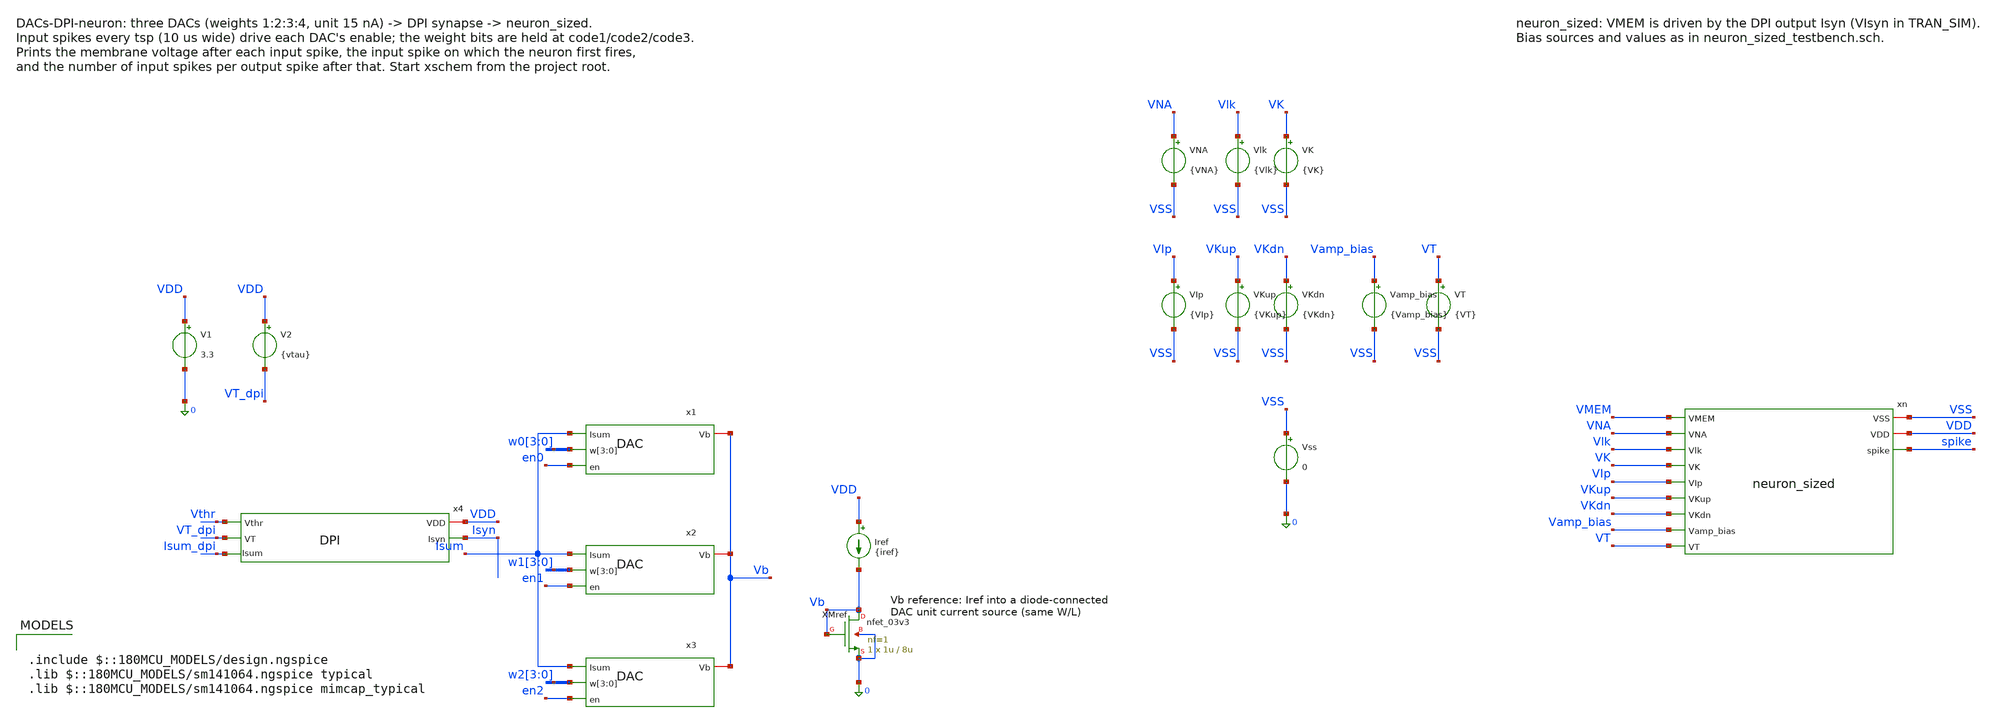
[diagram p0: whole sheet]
** sch_path: analog/neuron/DACs-DPI-neuron.sch
**.subckt DACs-DPI-neuron
x1 Isum Vb w0[3] w0[2] w0[1] w0[0] en0 DAC
x2 Isum Vb w1[3] w1[2] w1[1] w1[0] en1 DAC
x3 Isum Vb w2[3] w2[2] w2[1] w2[0] en2 DAC
x4 VDD Vthr Isyn Isum_dpi VT_dpi DPI
Iref VDD Vb {iref}
XMref Vb Vb 0 0 nfet_03v3 L=8u W=1u nf=1 ad='int((nf+1)/2) * W/nf * 0.18u' as='int((nf+2)/2) * W/nf * 0.18u'
+ pd='2*int((nf+1)/2) * (W/nf + 0.18u)' ps='2*int((nf+2)/2) * (W/nf + 0.18u)' nrd='0.18u / W' nrs='0.18u / W'
+ sa=0 sb=0 sd=0 m=1
V1 VDD 0 3.3
V2 VDD VT_dpi {vtau}
Vss VSS 0 0
xn VSS VDD VMEM VNA Vlk VK VIp VKup VKdn Vamp_bias VT spike neuron_sized
Vlk Vlk VSS {Vlk}
VK VK VSS {VK}
VNA VNA VSS {VNA}
VKup VKup VSS {VKup}
VKdn VKdn VSS {VKdn}
VIp VIp VSS {VIp}
VT VT VSS {VT}
Vamp_bias Vamp_bias VSS {Vamp_bias}
**** begin user architecture code

.include $::180MCU_MODELS/design.ngspice
.lib $::180MCU_MODELS/sm141064.ngspice typical
.lib $::180MCU_MODELS/sm141064.ngspice mimcap_typical



* How many input spikes of a given weight fire neuron_sized.
* One input spike of width tpw every tsp, from t0, on the enable (en) of each DAC.
* The weight bits of DACs x1 / x2 / x3 are held at code1 / code2 / code3 (0..15). DAC branch weights
*+ w[0]..w[3] = 1:2:3:4 with a 15 nA unit,
* so code 2 = weight 2 = 30 nA while the spike is high.
* vthr is tuned so that code 2 at 5 kHz (tsp = 200 us) first fires the neuron on input
* spike 10 (tt, 27 C). The count is steep in vthr: about one input spike per 1-2 mV.
.param vdd=3.3 vthr=2.909 vtau=0.40 iref=14.42n tpw=10u tsp=200u t0=100u
.param code1=2 code2=0 code3=0
* neuron_sized biases, as in neuron_sized_testbench.sch
.param Vlk=0.425 Vamp_bias=0.535 VIp=0.573 VNA=1.93 VKup=2.35 VK=1.22 VKdn=0.588 VT=1.66
* Bit b of each code
.param x1b0={code1-2*floor(code1/2)} x1b1={floor(code1/2)-2*floor(code1/4)}
.param x1b2={floor(code1/4)-2*floor(code1/8)} x1b3={floor(code1/8)-2*floor(code1/16)}
.param x2b0={code2-2*floor(code2/2)} x2b1={floor(code2/2)-2*floor(code2/4)}
.param x2b2={floor(code2/4)-2*floor(code2/8)} x2b3={floor(code2/8)-2*floor(code2/16)}
.param x3b0={code3-2*floor(code3/2)} x3b1={floor(code3/2)-2*floor(code3/4)}
.param x3b2={floor(code3/4)-2*floor(code3/8)} x3b3={floor(code3/8)-2*floor(code3/16)}
.csparam tsp_c={tsp}
.csparam t0_c={t0}
.csparam wsum_c={x1b0+2*x1b1+3*x1b2+4*x1b3 + x2b0+2*x2b1+3*x2b2+4*x2b3 + x3b0+2*x3b1+3*x3b2+4*x3b3}
.ic v(VMEM)=0 v(spike)=0
* Gear integration: the default (trap) makes i(VIsyn) ring step to step after each reset
.options method=gear

Vthr  Vthr 0 {vthr}
VIdac Isum_dpi Isum 0
* DPI output into the neuron membrane
VIsyn Isyn VMEM 0

* Weights are static levels, as from the weight register file: Vw<b><d> holds
* bit <b> of code<d+1> on DAC x<d+1> (net w<d>[<b>])
Vw00 w0[0] 0 {vdd*x1b0}
Vw10 w0[1] 0 {vdd*x1b1}
Vw20 w0[2] 0 {vdd*x1b2}
Vw30 w0[3] 0 {vdd*x1b3}
Vw01 w1[0] 0 {vdd*x2b0}
Vw11 w1[1] 0 {vdd*x2b1}
Vw21 w1[2] 0 {vdd*x2b2}
Vw31 w1[3] 0 {vdd*x2b3}
Vw02 w2[0] 0 {vdd*x3b0}
Vw12 w2[1] 0 {vdd*x3b1}
Vw22 w2[2] 0 {vdd*x3b2}
Vw32 w2[3] 0 {vdd*x3b3}

* Input spike train on each DAC's enable (the previous section's output)
Ven0 en0 0 pulse(0 {vdd} {t0} 10n 10n {tpw} {tsp})
Ven1 en1 0 pulse(0 {vdd} {t0} 10n 10n {tpw} {tsp})
Ven2 en2 0 pulse(0 {vdd} {t0} 10n 10n {tpw} {tsp})

.control
  save all
  set wr_singlescale
  set wr_vecnames
  tran 0.1u 6.1m 0 0.5u
  let isyn = i(VIsyn)
  let nin = floor((6.1m - t0_c)/tsp_c)
  let rate_khz = 1e-3/tsp_c
  echo
  echo Total weight per input spike: $&wsum_c, input rate $&rate_khz kHz, $&nin input spikes

  meas tran vsp max v(spike)
  let n_first = 0
  if vsp < 1.65
    echo The neuron did not fire.
    let nshow = nin
  else
    meas tran t1 when v(spike)=1.65 rise=1
    let n_first = floor((t1 - t0_c)/tsp_c) + 1
    let lat_us = (t1 - t0_c - (n_first - 1)*tsp_c)*1e6
    let nshow = n_first
    echo First output spike after input spike $&n_first ($&lat_us us after it).
  end

  * Membrane just before each next input spike, and the DPI peak in each interval
  echo
  echo input  VMEM_before_next(V)  Isyn_peak(nA)
  let k = 1
  while k <= nshow
    let ta = t0_c + (k - 1)*tsp_c
    let tb = t0_c + k*tsp_c - 1u
    meas tran m_v find v(VMEM) at=$&tb
    let tc = ta + 0.5*tsp_c
    meas tran m_i max isyn from=$&ta to=$&tc
    let i_na = m_i*1e9
    if k = n_first
      echo $&k  fired  $&i_na
    else
      echo $&k  $&m_v  $&i_na
    end
    let k = k + 1
  end

  * Input spikes per output spike once firing has started
  let t3 = 0
  if n_first > 0
    meas tran t3 when v(spike)=1.65 rise=3
  end
  let n_per = 0
  if t3 > 0
    let n_per = (t3 - t1)/(2*tsp_c)
    echo
    echo After the first output: one output spike every $&n_per input spikes.
  end

  * DAC charge per input spike (spike 2), with the DAC leakage between spikes removed
  let ta = t0_c + tsp_c
  let tm = ta + 0.5*tsp_c
  let te = ta + tsp_c - 1u
  meas tran m_q integ i(VIdac) from=$&ta to=$&tm
  meas tran m_lk avg i(VIdac) from=$&tm to=$&te
  let q_spike = m_q - m_lk*(tm - ta)
  let q_fc = q_spike*1e15
  let lk_pa = m_lk*1e12
  echo DAC charge per input spike: $&q_fc fC (DAC leakage between spikes $&lk_pa pA)
  echo RES q_spike=$&q_spike
  echo RES i_leak=$&m_lk

  echo RES n_first=$&n_first
  echo RES n_per=$&n_per

  wrdata dacs_dpi_neuron.txt v(VMEM) v(spike) isyn v(en0)
  if $?batchmode = 0
    plot v(VMEM) v(spike) v(en0)*0.15 title 'Membrane, output spike, input spikes on en0 (x0.15)' ylabel
+ 'V'
    plot isyn title 'DPI output current into the membrane' ylabel 'A'
  end
.endc


**** end user architecture code
**.ends

* expanding   symbol:  DAC.sym # of pins=4
** sym_path: analog/neuron/DAC.sym
** sch_path: analog/neuron/DAC.sch
.subckt DAC Isum Vb w[3] w[2] w[1] w[0] en
*.iopin Vb
*.ipin w[3],w[2],w[1],w[0]
*.ipin Isum
*.ipin en
XM1 X w[0] net4 net4 nfet_03v3 L=0.28u W=0.22u nf=1 ad='int((nf+1)/2) * W/nf * 0.18u' as='int((nf+2)/2) * W/nf * 0.18u'
+ pd='2*int((nf+1)/2) * (W/nf + 0.18u)' ps='2*int((nf+2)/2) * (W/nf + 0.18u)' nrd='0.18u / W' nrs='0.18u / W'
+ sa=0 sb=0 sd=0 m=1
XM2 net4 Vb GND GND nfet_03v3 L=8u W=1u nf=1 ad='int((nf+1)/2) * W/nf * 0.18u' as='int((nf+2)/2) * W/nf * 0.18u'
+ pd='2*int((nf+1)/2) * (W/nf + 0.18u)' ps='2*int((nf+2)/2) * (W/nf + 0.18u)' nrd='0.18u / W' nrs='0.18u / W'
+ sa=0 sb=0 sd=0 m=1
XM3 X w[1] net2 net2 nfet_03v3 L=0.28u W=0.22u nf=1 ad='int((nf+1)/2) * W/nf * 0.18u' as='int((nf+2)/2) * W/nf * 0.18u'
+ pd='2*int((nf+1)/2) * (W/nf + 0.18u)' ps='2*int((nf+2)/2) * (W/nf + 0.18u)' nrd='0.18u / W' nrs='0.18u / W'
+ sa=0 sb=0 sd=0 m=2
XM4 net2 Vb GND GND nfet_03v3 L=8u W=1u nf=1 ad='int((nf+1)/2) * W/nf * 0.18u' as='int((nf+2)/2) * W/nf * 0.18u'
+ pd='2*int((nf+1)/2) * (W/nf + 0.18u)' ps='2*int((nf+2)/2) * (W/nf + 0.18u)' nrd='0.18u / W' nrs='0.18u / W'
+ sa=0 sb=0 sd=0 m=2
XM5 X w[2] net3 net3 nfet_03v3 L=0.28u W=0.22u nf=1 ad='int((nf+1)/2) * W/nf * 0.18u' as='int((nf+2)/2) * W/nf * 0.18u'
+ pd='2*int((nf+1)/2) * (W/nf + 0.18u)' ps='2*int((nf+2)/2) * (W/nf + 0.18u)' nrd='0.18u / W' nrs='0.18u / W'
+ sa=0 sb=0 sd=0 m=3
XM6 net3 Vb GND GND nfet_03v3 L=8u W=1u nf=1 ad='int((nf+1)/2) * W/nf * 0.18u' as='int((nf+2)/2) * W/nf * 0.18u'
+ pd='2*int((nf+1)/2) * (W/nf + 0.18u)' ps='2*int((nf+2)/2) * (W/nf + 0.18u)' nrd='0.18u / W' nrs='0.18u / W'
+ sa=0 sb=0 sd=0 m=3
XM7 X w[3] net1 net1 nfet_03v3 L=0.28u W=0.22u nf=1 ad='int((nf+1)/2) * W/nf * 0.18u' as='int((nf+2)/2) * W/nf * 0.18u'
+ pd='2*int((nf+1)/2) * (W/nf + 0.18u)' ps='2*int((nf+2)/2) * (W/nf + 0.18u)' nrd='0.18u / W' nrs='0.18u / W'
+ sa=0 sb=0 sd=0 m=4
XM8 net1 Vb GND GND nfet_03v3 L=8u W=1u nf=1 ad='int((nf+1)/2) * W/nf * 0.18u' as='int((nf+2)/2) * W/nf * 0.18u'
+ pd='2*int((nf+1)/2) * (W/nf + 0.18u)' ps='2*int((nf+2)/2) * (W/nf + 0.18u)' nrd='0.18u / W' nrs='0.18u / W'
+ sa=0 sb=0 sd=0 m=4
XMen Isum en X GND nfet_03v3 L=0.28u W=0.22u nf=1 ad='int((nf+1)/2) * W/nf * 0.18u' as='int((nf+2)/2) * W/nf * 0.18u'
+ pd='2*int((nf+1)/2) * (W/nf + 0.18u)' ps='2*int((nf+2)/2) * (W/nf + 0.18u)' nrd='0.18u / W' nrs='0.18u / W'
+ sa=0 sb=0 sd=0 m=1
.ends


* expanding   symbol:  DPI.sym # of pins=5
** sym_path: analog/neuron/DPI.sym
** sch_path: analog/neuron/DPI.sch
.subckt DPI VDD Vthr Isyn Isum VT
*.ipin Vthr
*.iopin VDD
*.opin Isyn
*.opin Isum
*.ipin VT
XM1 VDD Vthr Isum Isum nfet_03v3 L=0.28u W=0.22u nf=1 ad='int((nf+1)/2) * W/nf * 0.18u' as='int((nf+2)/2) * W/nf * 0.18u'
+ pd='2*int((nf+1)/2) * (W/nf + 0.18u)' ps='2*int((nf+2)/2) * (W/nf + 0.18u)' nrd='0.18u / W' nrs='0.18u / W'
+ sa=0 sb=0 sd=0 m=1
XM2 net1 net1 Isum Isum nfet_03v3 L=0.28u W=0.22u nf=1 ad='int((nf+1)/2) * W/nf * 0.18u' as='int((nf+2)/2) * W/nf * 0.18u'
+ pd='2*int((nf+1)/2) * (W/nf + 0.18u)' ps='2*int((nf+2)/2) * (W/nf + 0.18u)' nrd='0.18u / W' nrs='0.18u / W'
+ sa=0 sb=0 sd=0 m=1
XM3 net1 VT VDD VDD pfet_03v3 L=0.28u W=0.22u nf=1 ad='int((nf+1)/2) * W/nf * 0.18u' as='int((nf+2)/2) * W/nf * 0.18u'
+ pd='2*int((nf+1)/2) * (W/nf + 0.18u)' ps='2*int((nf+2)/2) * (W/nf + 0.18u)' nrd='0.18u / W' nrs='0.18u / W'
+ sa=0 sb=0 sd=0 m=1
XM4 Isyn net1 VDD VDD pfet_03v3 L=0.28u W=0.22u nf=1 ad='int((nf+1)/2) * W/nf * 0.18u' as='int((nf+2)/2) * W/nf * 0.18u'
+ pd='2*int((nf+1)/2) * (W/nf + 0.18u)' ps='2*int((nf+2)/2) * (W/nf + 0.18u)' nrd='0.18u / W' nrs='0.18u / W'
+ sa=0 sb=0 sd=0 m=1
C4 VDD net1 1p m=1
.ends


* expanding   symbol:  neuron_sized.sym # of pins=12
** sym_path: analog/neuron/neuron_sized.sym
** sch_path: analog/neuron/neuron_sized.sch
.subckt neuron_sized VSS VDD VMEM VNA Vlk VK VIp VKup VKdn Vamp_bias VT spike
*.iopin VSS
*.iopin VDD
*.ipin VMEM
*.ipin VNA
*.ipin Vlk
*.ipin VK
*.ipin VIp
*.ipin VKup
*.ipin VKdn
*.opin spike
*.ipin Vamp_bias
*.ipin VT
x1 VDD VSS VMEM VT Vamp_bias net1 spike_amplifier
XM1 net2 net1 net4 VSS nfet_03v3 L=0.28u W=0.22u nf=1 ad='int((nf+1)/2) * W/nf * 0.18u' as='int((nf+2)/2) * W/nf * 0.18u'
+ pd='2*int((nf+1)/2) * (W/nf + 0.18u)' ps='2*int((nf+2)/2) * (W/nf + 0.18u)' nrd='0.18u / W' nrs='0.18u / W'
+ sa=0 sb=0 sd=0 m=1
XM2 spike net2 net5 VSS nfet_03v3 L=0.28u W=0.22u nf=1 ad='int((nf+1)/2) * W/nf * 0.18u' as='int((nf+2)/2) * W/nf * 0.18u'
+ pd='2*int((nf+1)/2) * (W/nf + 0.18u)' ps='2*int((nf+2)/2) * (W/nf + 0.18u)' nrd='0.18u / W' nrs='0.18u / W'
+ sa=0 sb=0 sd=0 m=1
XM3 net2 net1 VDD VDD pfet_03v3 L=0.28u W=0.22u nf=1 ad='int((nf+1)/2) * W/nf * 0.18u' as='int((nf+2)/2) * W/nf * 0.18u'
+ pd='2*int((nf+1)/2) * (W/nf + 0.18u)' ps='2*int((nf+2)/2) * (W/nf + 0.18u)' nrd='0.18u / W' nrs='0.18u / W'
+ sa=0 sb=0 sd=0 m=1
XM4 spike net2 net3 VDD pfet_03v3 L=0.28u W=0.22u nf=1 ad='int((nf+1)/2) * W/nf * 0.18u' as='int((nf+2)/2) * W/nf * 0.18u'
+ pd='2*int((nf+1)/2) * (W/nf + 0.18u)' ps='2*int((nf+2)/2) * (W/nf + 0.18u)' nrd='0.18u / W' nrs='0.18u / W'
+ sa=0 sb=0 sd=0 m=1
XM5 VMEM net2 net7 VDD pfet_03v3 L=0.28u W=0.22u nf=1 ad='int((nf+1)/2) * W/nf * 0.18u' as='int((nf+2)/2) * W/nf * 0.18u'
+ pd='2*int((nf+1)/2) * (W/nf + 0.18u)' ps='2*int((nf+2)/2) * (W/nf + 0.18u)' nrd='0.18u / W' nrs='0.18u / W'
+ sa=0 sb=0 sd=0 m=1
XM6 VMEM spike net6 VSS nfet_03v3 L=5u W=0.22u nf=1 ad='int((nf+1)/2) * W/nf * 0.18u' as='int((nf+2)/2) * W/nf * 0.18u'
+ pd='2*int((nf+1)/2) * (W/nf + 0.18u)' ps='2*int((nf+2)/2) * (W/nf + 0.18u)' nrd='0.18u / W' nrs='0.18u / W'
+ sa=0 sb=0 sd=0 m=1
XC1 spike VSS cap_mim_2f0_m3m4_noshield c_width=10e-6 c_length=10e-6 m=1
XM7 net5 VKdn VSS VSS nfet_03v3 L=1u W=1u nf=1 ad='int((nf+1)/2) * W/nf * 0.18u' as='int((nf+2)/2) * W/nf * 0.18u'
+ pd='2*int((nf+1)/2) * (W/nf + 0.18u)' ps='2*int((nf+2)/2) * (W/nf + 0.18u)' nrd='0.18u / W' nrs='0.18u / W'
+ sa=0 sb=0 sd=0 m=1
XM8 net4 VIp VSS VSS nfet_03v3 L=1u W=1u nf=1 ad='int((nf+1)/2) * W/nf * 0.18u' as='int((nf+2)/2) * W/nf * 0.18u'
+ pd='2*int((nf+1)/2) * (W/nf + 0.18u)' ps='2*int((nf+2)/2) * (W/nf + 0.18u)' nrd='0.18u / W' nrs='0.18u / W'
+ sa=0 sb=0 sd=0 m=1
XM9 net7 VNA VDD VDD pfet_03v3 L=1u W=1u nf=1 ad='int((nf+1)/2) * W/nf * 0.18u' as='int((nf+2)/2) * W/nf * 0.18u'
+ pd='2*int((nf+1)/2) * (W/nf + 0.18u)' ps='2*int((nf+2)/2) * (W/nf + 0.18u)' nrd='0.18u / W' nrs='0.18u / W'
+ sa=0 sb=0 sd=0 m=1
XM10 net6 VK VSS VSS nfet_03v3 L=1u W=1u nf=1 ad='int((nf+1)/2) * W/nf * 0.18u' as='int((nf+2)/2) * W/nf * 0.18u'
+ pd='2*int((nf+1)/2) * (W/nf + 0.18u)' ps='2*int((nf+2)/2) * (W/nf + 0.18u)' nrd='0.18u / W' nrs='0.18u / W'
+ sa=0 sb=0 sd=0 m=1
XC2 VMEM VSS cap_mim_2f0_m3m4_noshield c_width=22.18e-6 c_length=22.18e-6 m=1
XM11 VMEM Vlk VSS VSS nfet_03v3 L=1u W=1u nf=1 ad='int((nf+1)/2) * W/nf * 0.18u' as='int((nf+2)/2) * W/nf * 0.18u'
+ pd='2*int((nf+1)/2) * (W/nf + 0.18u)' ps='2*int((nf+2)/2) * (W/nf + 0.18u)' nrd='0.18u / W' nrs='0.18u / W'
+ sa=0 sb=0 sd=0 m=1
XM12 net3 VKup VDD VDD pfet_03v3 L=1u W=1u nf=1 ad='int((nf+1)/2) * W/nf * 0.18u' as='int((nf+2)/2) * W/nf * 0.18u'
+ pd='2*int((nf+1)/2) * (W/nf + 0.18u)' ps='2*int((nf+2)/2) * (W/nf + 0.18u)' nrd='0.18u / W' nrs='0.18u / W'
+ sa=0 sb=0 sd=0 m=1
.ends


* expanding   symbol:  spike_amplifier.sym # of pins=6
** sym_path: analog/neuron/spike_amplifier.sym
** sch_path: analog/neuron/spike_amplifier.sch
.subckt spike_amplifier VDD VSS VP VN VB spike_out
*.iopin VDD
*.iopin VSS
*.ipin VP
*.ipin VN
*.ipin VB
*.opin spike_out
XM1 net2 VP net1 VSS nfet_03v3 L=0.28u W=0.22u nf=1 ad='int((nf+1)/2) * W/nf * 0.18u' as='int((nf+2)/2) * W/nf * 0.18u'
+ pd='2*int((nf+1)/2) * (W/nf + 0.18u)' ps='2*int((nf+2)/2) * (W/nf + 0.18u)' nrd='0.18u / W' nrs='0.18u / W'
+ sa=0 sb=0 sd=0 m=1
XM2 spike_out VN net1 VSS nfet_03v3 L=0.28u W=0.22u nf=1 ad='int((nf+1)/2) * W/nf * 0.18u' as='int((nf+2)/2) * W/nf * 0.18u'
+ pd='2*int((nf+1)/2) * (W/nf + 0.18u)' ps='2*int((nf+2)/2) * (W/nf + 0.18u)' nrd='0.18u / W' nrs='0.18u / W'
+ sa=0 sb=0 sd=0 m=1
XM3 net1 VB VSS VSS nfet_03v3 L=0.28u W=0.22u nf=1 ad='int((nf+1)/2) * W/nf * 0.18u' as='int((nf+2)/2) * W/nf * 0.18u'
+ pd='2*int((nf+1)/2) * (W/nf + 0.18u)' ps='2*int((nf+2)/2) * (W/nf + 0.18u)' nrd='0.18u / W' nrs='0.18u / W'
+ sa=0 sb=0 sd=0 m=1
XM4 net2 net2 VDD VDD pfet_03v3 L=0.28u W=0.22u nf=1 ad='int((nf+1)/2) * W/nf * 0.18u' as='int((nf+2)/2) * W/nf * 0.18u'
+ pd='2*int((nf+1)/2) * (W/nf + 0.18u)' ps='2*int((nf+2)/2) * (W/nf + 0.18u)' nrd='0.18u / W' nrs='0.18u / W'
+ sa=0 sb=0 sd=0 m=1
XM5 spike_out net2 VDD VDD pfet_03v3 L=0.28u W=0.22u nf=1 ad='int((nf+1)/2) * W/nf * 0.18u' as='int((nf+2)/2) * W/nf * 0.18u'
+ pd='2*int((nf+1)/2) * (W/nf + 0.18u)' ps='2*int((nf+2)/2) * (W/nf + 0.18u)' nrd='0.18u / W' nrs='0.18u / W'
+ sa=0 sb=0 sd=0 m=1
.ends

.GLOBAL GND
.end
